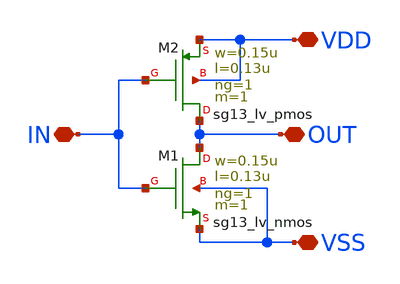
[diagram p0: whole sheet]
** sch_path: blocks/inverter/schematic/inverter.sch
* Copyright 2023  IHP PDK Authors
* Licensed under the Apache License, Version 2.0 (the "License");
* you may not use this file except in compliance with the License.
* You may obtain a copy of the License at
* https://www.apache.org/licenses/LICENSE-2.0
* Unless required by applicable law or agreed to in writing, software
* distributed under the License is distributed on an "AS IS" BASIS,
* WITHOUT WARRANTIES OR CONDITIONS OF ANY KIND, either express or implied.
* See the License for the specific language governing permissions and
* limitations under the License.
**.subckt inverter IN OUT VDD VSS
*.iopin IN
*.iopin OUT
*.iopin VDD
*.iopin VSS
XM1 OUT IN VSS VSS sg13_lv_nmos w=0.15u l=0.13u ng=1 m=1 mm_ok=1
XM2 OUT IN VDD VDD sg13_lv_pmos w=0.15u l=0.13u ng=1 m=1 mm_ok=1
**.ends
.end
